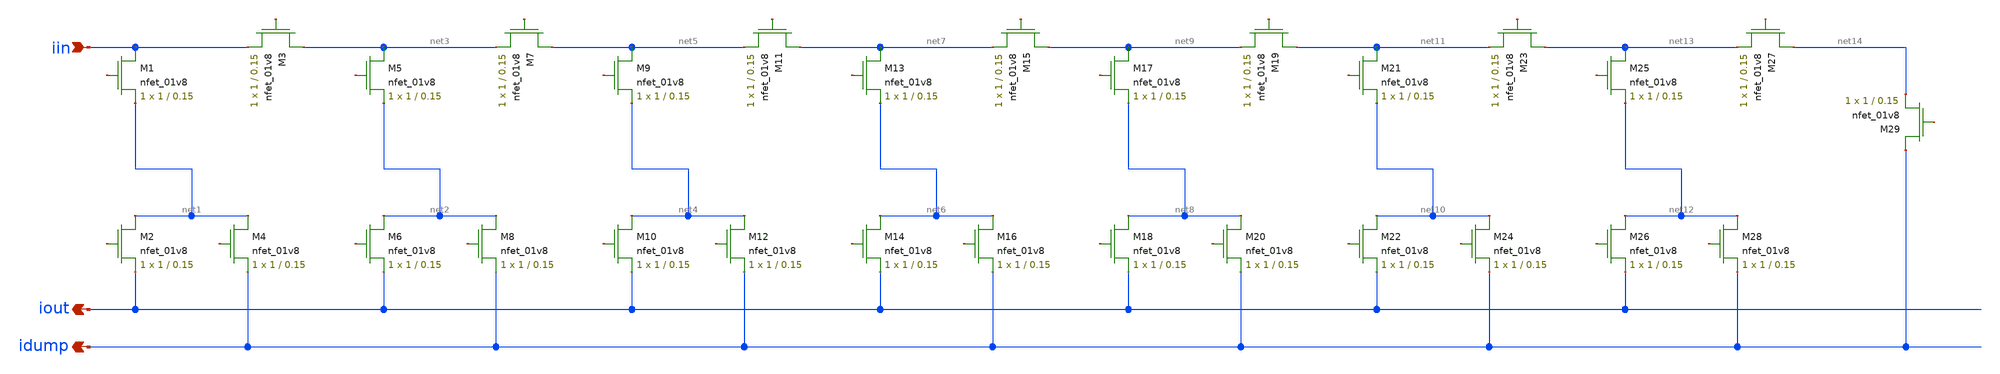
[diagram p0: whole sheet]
** sch_path: schematic/ladder.sch
**.subckt ladder iout idump iin
*.opin iout
*.opin idump
*.ipin iin
XM1 iin net15 net1 GND sky130_fd_pr__nfet_01v8 L=0.15 W=1 nf=1 ad='int((nf+1)/2) * W/nf * 0.29' as='int((nf+2)/2) * W/nf * 0.29'
+ pd='2*int((nf+1)/2) * (W/nf + 0.29)' ps='2*int((nf+2)/2) * (W/nf + 0.29)' nrd='0.29 / W' nrs='0.29 / W'
+ sa=0 sb=0 sd=0 mult=1 m=1
XM2 net1 net16 iout GND sky130_fd_pr__nfet_01v8 L=0.15 W=1 nf=1 ad='int((nf+1)/2) * W/nf * 0.29' as='int((nf+2)/2) * W/nf * 0.29'
+ pd='2*int((nf+1)/2) * (W/nf + 0.29)' ps='2*int((nf+2)/2) * (W/nf + 0.29)' nrd='0.29 / W' nrs='0.29 / W'
+ sa=0 sb=0 sd=0 mult=1 m=1
XM3 net3 net17 iin GND sky130_fd_pr__nfet_01v8 L=0.15 W=1 nf=1 ad='int((nf+1)/2) * W/nf * 0.29' as='int((nf+2)/2) * W/nf * 0.29'
+ pd='2*int((nf+1)/2) * (W/nf + 0.29)' ps='2*int((nf+2)/2) * (W/nf + 0.29)' nrd='0.29 / W' nrs='0.29 / W'
+ sa=0 sb=0 sd=0 mult=1 m=1
XM4 net1 net18 idump GND sky130_fd_pr__nfet_01v8 L=0.15 W=1 nf=1 ad='int((nf+1)/2) * W/nf * 0.29' as='int((nf+2)/2) * W/nf * 0.29'
+ pd='2*int((nf+1)/2) * (W/nf + 0.29)' ps='2*int((nf+2)/2) * (W/nf + 0.29)' nrd='0.29 / W' nrs='0.29 / W'
+ sa=0 sb=0 sd=0 mult=1 m=1
XM5 net3 net19 net2 GND sky130_fd_pr__nfet_01v8 L=0.15 W=1 nf=1 ad='int((nf+1)/2) * W/nf * 0.29' as='int((nf+2)/2) * W/nf * 0.29'
+ pd='2*int((nf+1)/2) * (W/nf + 0.29)' ps='2*int((nf+2)/2) * (W/nf + 0.29)' nrd='0.29 / W' nrs='0.29 / W'
+ sa=0 sb=0 sd=0 mult=1 m=1
XM6 net2 net20 iout GND sky130_fd_pr__nfet_01v8 L=0.15 W=1 nf=1 ad='int((nf+1)/2) * W/nf * 0.29' as='int((nf+2)/2) * W/nf * 0.29'
+ pd='2*int((nf+1)/2) * (W/nf + 0.29)' ps='2*int((nf+2)/2) * (W/nf + 0.29)' nrd='0.29 / W' nrs='0.29 / W'
+ sa=0 sb=0 sd=0 mult=1 m=1
XM7 net5 net21 net3 GND sky130_fd_pr__nfet_01v8 L=0.15 W=1 nf=1 ad='int((nf+1)/2) * W/nf * 0.29' as='int((nf+2)/2) * W/nf * 0.29'
+ pd='2*int((nf+1)/2) * (W/nf + 0.29)' ps='2*int((nf+2)/2) * (W/nf + 0.29)' nrd='0.29 / W' nrs='0.29 / W'
+ sa=0 sb=0 sd=0 mult=1 m=1
XM8 net2 net22 idump GND sky130_fd_pr__nfet_01v8 L=0.15 W=1 nf=1 ad='int((nf+1)/2) * W/nf * 0.29' as='int((nf+2)/2) * W/nf * 0.29'
+ pd='2*int((nf+1)/2) * (W/nf + 0.29)' ps='2*int((nf+2)/2) * (W/nf + 0.29)' nrd='0.29 / W' nrs='0.29 / W'
+ sa=0 sb=0 sd=0 mult=1 m=1
XM9 net5 net23 net4 GND sky130_fd_pr__nfet_01v8 L=0.15 W=1 nf=1 ad='int((nf+1)/2) * W/nf * 0.29' as='int((nf+2)/2) * W/nf * 0.29'
+ pd='2*int((nf+1)/2) * (W/nf + 0.29)' ps='2*int((nf+2)/2) * (W/nf + 0.29)' nrd='0.29 / W' nrs='0.29 / W'
+ sa=0 sb=0 sd=0 mult=1 m=1
XM10 net4 net24 iout GND sky130_fd_pr__nfet_01v8 L=0.15 W=1 nf=1 ad='int((nf+1)/2) * W/nf * 0.29' as='int((nf+2)/2) * W/nf * 0.29'
+ pd='2*int((nf+1)/2) * (W/nf + 0.29)' ps='2*int((nf+2)/2) * (W/nf + 0.29)' nrd='0.29 / W' nrs='0.29 / W'
+ sa=0 sb=0 sd=0 mult=1 m=1
XM11 net7 net25 net5 GND sky130_fd_pr__nfet_01v8 L=0.15 W=1 nf=1 ad='int((nf+1)/2) * W/nf * 0.29' as='int((nf+2)/2) * W/nf * 0.29'
+ pd='2*int((nf+1)/2) * (W/nf + 0.29)' ps='2*int((nf+2)/2) * (W/nf + 0.29)' nrd='0.29 / W' nrs='0.29 / W'
+ sa=0 sb=0 sd=0 mult=1 m=1
XM12 net4 net26 idump GND sky130_fd_pr__nfet_01v8 L=0.15 W=1 nf=1 ad='int((nf+1)/2) * W/nf * 0.29' as='int((nf+2)/2) * W/nf * 0.29'
+ pd='2*int((nf+1)/2) * (W/nf + 0.29)' ps='2*int((nf+2)/2) * (W/nf + 0.29)' nrd='0.29 / W' nrs='0.29 / W'
+ sa=0 sb=0 sd=0 mult=1 m=1
XM13 net7 net27 net6 GND sky130_fd_pr__nfet_01v8 L=0.15 W=1 nf=1 ad='int((nf+1)/2) * W/nf * 0.29' as='int((nf+2)/2) * W/nf * 0.29'
+ pd='2*int((nf+1)/2) * (W/nf + 0.29)' ps='2*int((nf+2)/2) * (W/nf + 0.29)' nrd='0.29 / W' nrs='0.29 / W'
+ sa=0 sb=0 sd=0 mult=1 m=1
XM14 net6 net28 iout GND sky130_fd_pr__nfet_01v8 L=0.15 W=1 nf=1 ad='int((nf+1)/2) * W/nf * 0.29' as='int((nf+2)/2) * W/nf * 0.29'
+ pd='2*int((nf+1)/2) * (W/nf + 0.29)' ps='2*int((nf+2)/2) * (W/nf + 0.29)' nrd='0.29 / W' nrs='0.29 / W'
+ sa=0 sb=0 sd=0 mult=1 m=1
XM15 net9 net29 net7 GND sky130_fd_pr__nfet_01v8 L=0.15 W=1 nf=1 ad='int((nf+1)/2) * W/nf * 0.29' as='int((nf+2)/2) * W/nf * 0.29'
+ pd='2*int((nf+1)/2) * (W/nf + 0.29)' ps='2*int((nf+2)/2) * (W/nf + 0.29)' nrd='0.29 / W' nrs='0.29 / W'
+ sa=0 sb=0 sd=0 mult=1 m=1
XM16 net6 net30 idump GND sky130_fd_pr__nfet_01v8 L=0.15 W=1 nf=1 ad='int((nf+1)/2) * W/nf * 0.29' as='int((nf+2)/2) * W/nf * 0.29'
+ pd='2*int((nf+1)/2) * (W/nf + 0.29)' ps='2*int((nf+2)/2) * (W/nf + 0.29)' nrd='0.29 / W' nrs='0.29 / W'
+ sa=0 sb=0 sd=0 mult=1 m=1
XM17 net9 net31 net8 GND sky130_fd_pr__nfet_01v8 L=0.15 W=1 nf=1 ad='int((nf+1)/2) * W/nf * 0.29' as='int((nf+2)/2) * W/nf * 0.29'
+ pd='2*int((nf+1)/2) * (W/nf + 0.29)' ps='2*int((nf+2)/2) * (W/nf + 0.29)' nrd='0.29 / W' nrs='0.29 / W'
+ sa=0 sb=0 sd=0 mult=1 m=1
XM18 net8 net32 iout GND sky130_fd_pr__nfet_01v8 L=0.15 W=1 nf=1 ad='int((nf+1)/2) * W/nf * 0.29' as='int((nf+2)/2) * W/nf * 0.29'
+ pd='2*int((nf+1)/2) * (W/nf + 0.29)' ps='2*int((nf+2)/2) * (W/nf + 0.29)' nrd='0.29 / W' nrs='0.29 / W'
+ sa=0 sb=0 sd=0 mult=1 m=1
XM19 net11 net33 net9 GND sky130_fd_pr__nfet_01v8 L=0.15 W=1 nf=1 ad='int((nf+1)/2) * W/nf * 0.29' as='int((nf+2)/2) * W/nf * 0.29'
+ pd='2*int((nf+1)/2) * (W/nf + 0.29)' ps='2*int((nf+2)/2) * (W/nf + 0.29)' nrd='0.29 / W' nrs='0.29 / W'
+ sa=0 sb=0 sd=0 mult=1 m=1
XM20 net8 net34 idump GND sky130_fd_pr__nfet_01v8 L=0.15 W=1 nf=1 ad='int((nf+1)/2) * W/nf * 0.29' as='int((nf+2)/2) * W/nf * 0.29'
+ pd='2*int((nf+1)/2) * (W/nf + 0.29)' ps='2*int((nf+2)/2) * (W/nf + 0.29)' nrd='0.29 / W' nrs='0.29 / W'
+ sa=0 sb=0 sd=0 mult=1 m=1
XM21 net11 net35 net10 GND sky130_fd_pr__nfet_01v8 L=0.15 W=1 nf=1 ad='int((nf+1)/2) * W/nf * 0.29' as='int((nf+2)/2) * W/nf * 0.29'
+ pd='2*int((nf+1)/2) * (W/nf + 0.29)' ps='2*int((nf+2)/2) * (W/nf + 0.29)' nrd='0.29 / W' nrs='0.29 / W'
+ sa=0 sb=0 sd=0 mult=1 m=1
XM22 net10 net36 iout GND sky130_fd_pr__nfet_01v8 L=0.15 W=1 nf=1 ad='int((nf+1)/2) * W/nf * 0.29' as='int((nf+2)/2) * W/nf * 0.29'
+ pd='2*int((nf+1)/2) * (W/nf + 0.29)' ps='2*int((nf+2)/2) * (W/nf + 0.29)' nrd='0.29 / W' nrs='0.29 / W'
+ sa=0 sb=0 sd=0 mult=1 m=1
XM23 net13 net37 net11 GND sky130_fd_pr__nfet_01v8 L=0.15 W=1 nf=1 ad='int((nf+1)/2) * W/nf * 0.29' as='int((nf+2)/2) * W/nf * 0.29'
+ pd='2*int((nf+1)/2) * (W/nf + 0.29)' ps='2*int((nf+2)/2) * (W/nf + 0.29)' nrd='0.29 / W' nrs='0.29 / W'
+ sa=0 sb=0 sd=0 mult=1 m=1
XM24 net10 net38 idump GND sky130_fd_pr__nfet_01v8 L=0.15 W=1 nf=1 ad='int((nf+1)/2) * W/nf * 0.29' as='int((nf+2)/2) * W/nf * 0.29'
+ pd='2*int((nf+1)/2) * (W/nf + 0.29)' ps='2*int((nf+2)/2) * (W/nf + 0.29)' nrd='0.29 / W' nrs='0.29 / W'
+ sa=0 sb=0 sd=0 mult=1 m=1
XM25 net13 net39 net12 GND sky130_fd_pr__nfet_01v8 L=0.15 W=1 nf=1 ad='int((nf+1)/2) * W/nf * 0.29' as='int((nf+2)/2) * W/nf * 0.29'
+ pd='2*int((nf+1)/2) * (W/nf + 0.29)' ps='2*int((nf+2)/2) * (W/nf + 0.29)' nrd='0.29 / W' nrs='0.29 / W'
+ sa=0 sb=0 sd=0 mult=1 m=1
XM26 net12 net40 iout GND sky130_fd_pr__nfet_01v8 L=0.15 W=1 nf=1 ad='int((nf+1)/2) * W/nf * 0.29' as='int((nf+2)/2) * W/nf * 0.29'
+ pd='2*int((nf+1)/2) * (W/nf + 0.29)' ps='2*int((nf+2)/2) * (W/nf + 0.29)' nrd='0.29 / W' nrs='0.29 / W'
+ sa=0 sb=0 sd=0 mult=1 m=1
XM27 net14 net41 net13 GND sky130_fd_pr__nfet_01v8 L=0.15 W=1 nf=1 ad='int((nf+1)/2) * W/nf * 0.29' as='int((nf+2)/2) * W/nf * 0.29'
+ pd='2*int((nf+1)/2) * (W/nf + 0.29)' ps='2*int((nf+2)/2) * (W/nf + 0.29)' nrd='0.29 / W' nrs='0.29 / W'
+ sa=0 sb=0 sd=0 mult=1 m=1
XM28 net12 net42 idump GND sky130_fd_pr__nfet_01v8 L=0.15 W=1 nf=1 ad='int((nf+1)/2) * W/nf * 0.29' as='int((nf+2)/2) * W/nf * 0.29'
+ pd='2*int((nf+1)/2) * (W/nf + 0.29)' ps='2*int((nf+2)/2) * (W/nf + 0.29)' nrd='0.29 / W' nrs='0.29 / W'
+ sa=0 sb=0 sd=0 mult=1 m=1
XM29 idump net43 net14 GND sky130_fd_pr__nfet_01v8 L=0.15 W=1 nf=1 ad='int((nf+1)/2) * W/nf * 0.29' as='int((nf+2)/2) * W/nf * 0.29'
+ pd='2*int((nf+1)/2) * (W/nf + 0.29)' ps='2*int((nf+2)/2) * (W/nf + 0.29)' nrd='0.29 / W' nrs='0.29 / W'
+ sa=0 sb=0 sd=0 mult=1 m=1
**.ends
.end
